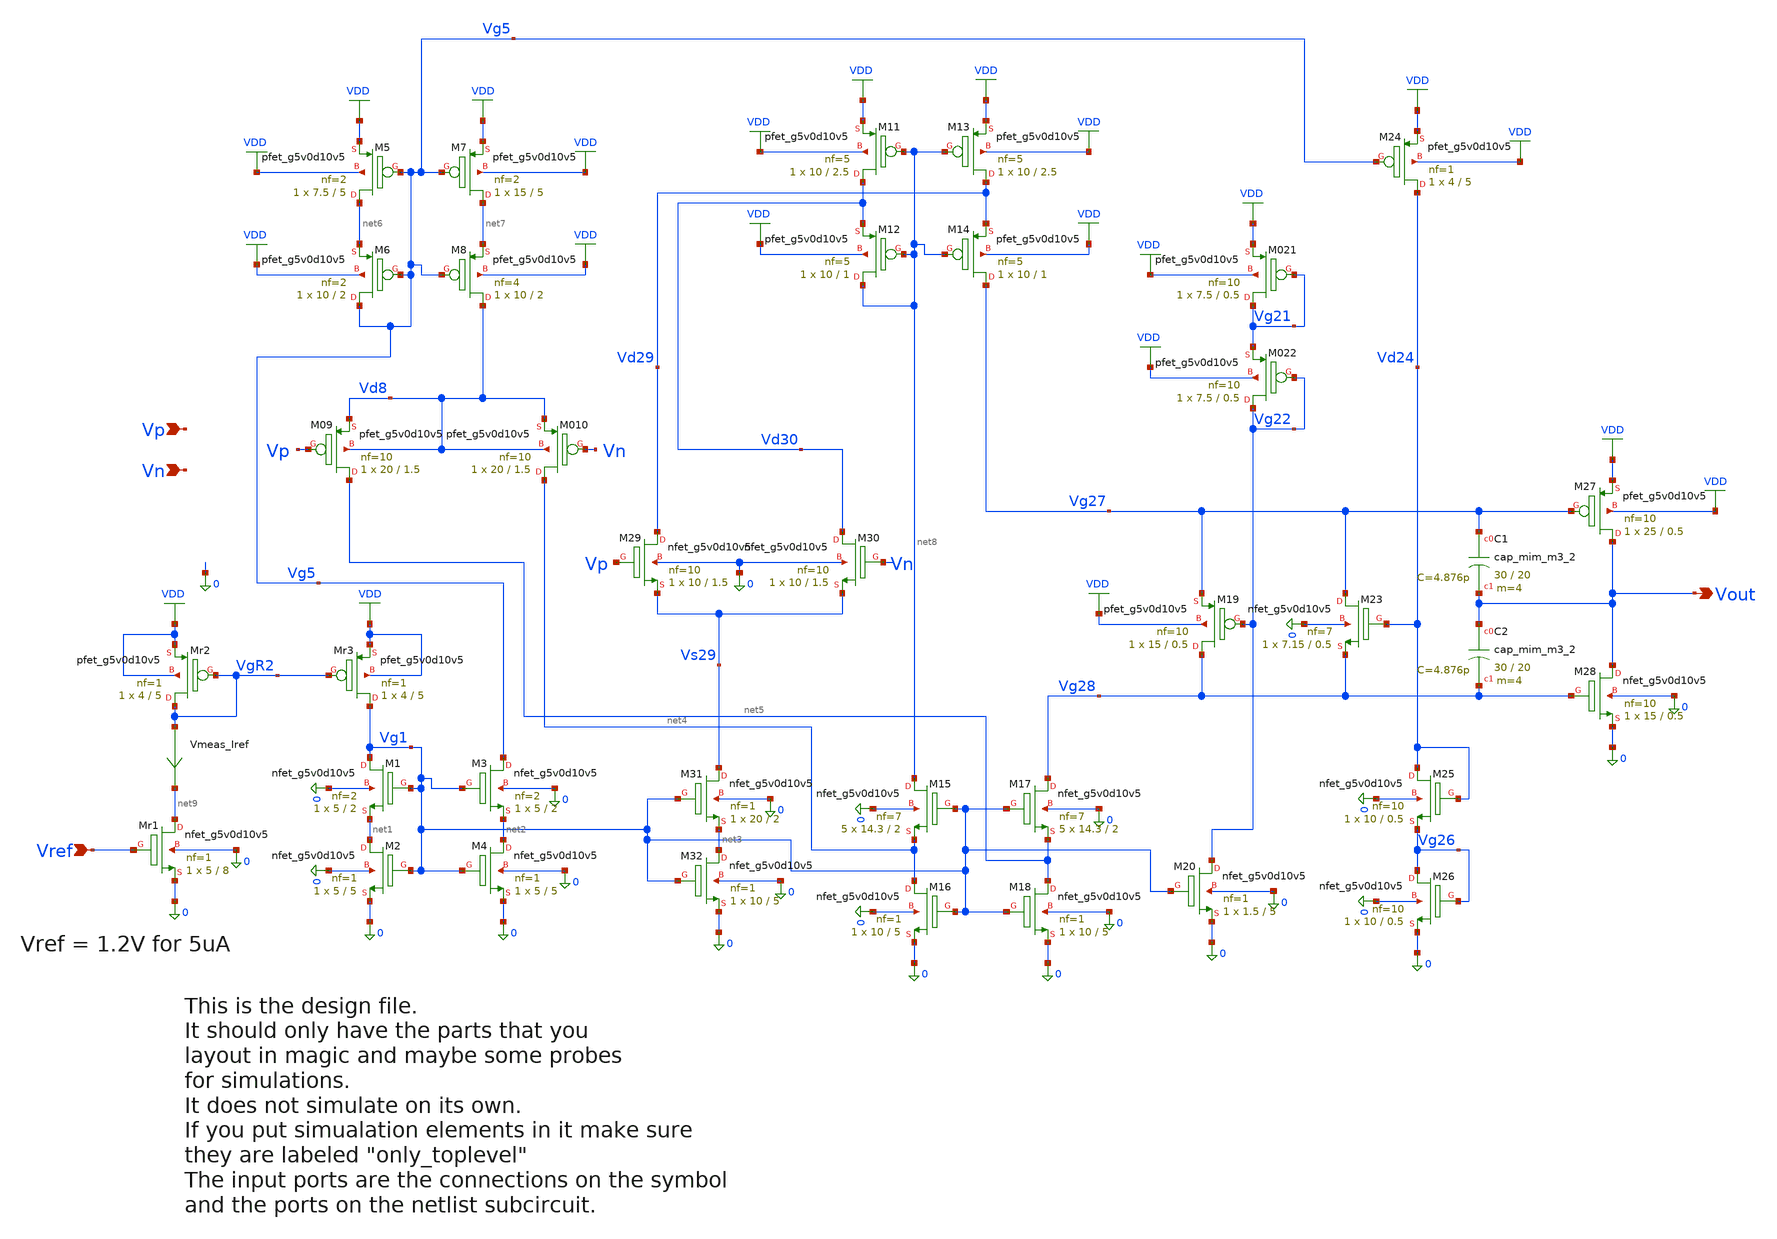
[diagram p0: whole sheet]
** sch_path: xschem/opamp_x_broken.sch
* Copyright 2021 Stefan Frederik Schippers
* Licensed under the Apache License, Version 2.0 (the "License");
* you may not use this file except in compliance with the License.
* You may obtain a copy of the License at
* https://www.apache.org/licenses/LICENSE-2.0
* Unless required by applicable law or agreed to in writing, software
* distributed under the License is distributed on an "AS IS" BASIS,
* WITHOUT WARRANTIES OR CONDITIONS OF ANY KIND, either express or implied.
* See the License for the specific language governing permissions and
* limitations under the License.
**.subckt opamp_x_broken Vout Vref Vp Vn
*.opin Vout
*.ipin Vref
*.ipin Vp
*.ipin Vn
XM1 Vg1 Vg1 net1 0 sky130_fd_pr__nfet_g5v0d10v5 L=2 W=5 nf=2 ad='int((2 + 1)/2) * 5 / 2 * 0.29' as='int((2 + 2)/2) * 5 / 2 * 0.29'
+ pd='2*int((2 + 1)/2) * (5 / 2 + 0.29)' ps='2*int((2 + 2)/2) * (5 / 2 + 0.29)' nrd='0.29 / 5 ' nrs='0.29 / 5 '
+ sa=0 sb=0 sd=0 mult=1 m=1
XM2 net1 Vg1 0 0 sky130_fd_pr__nfet_g5v0d10v5 L=5 W=5 nf=1 ad='int((1 + 1)/2) * 5 / 1 * 0.29' as='int((1 + 2)/2) * 5 / 1 * 0.29'
+ pd='2*int((1 + 1)/2) * (5 / 1 + 0.29)' ps='2*int((1 + 2)/2) * (5 / 1 + 0.29)' nrd='0.29 / 5 ' nrs='0.29 / 5 '
+ sa=0 sb=0 sd=0 mult=1 m=1
XM4 net2 Vg1 0 0 sky130_fd_pr__nfet_g5v0d10v5 L=5 W=5 nf=1 ad='int((1 + 1)/2) * 5 / 1 * 0.29' as='int((1 + 2)/2) * 5 / 1 * 0.29'
+ pd='2*int((1 + 1)/2) * (5 / 1 + 0.29)' ps='2*int((1 + 2)/2) * (5 / 1 + 0.29)' nrd='0.29 / 5 ' nrs='0.29 / 5 '
+ sa=0 sb=0 sd=0 mult=1 m=1
XM3 Vg5 Vg1 net2 0 sky130_fd_pr__nfet_g5v0d10v5 L=2 W=5 nf=2 ad='int((2 + 1)/2) * 5 / 2 * 0.29' as='int((2 + 2)/2) * 5 / 2 * 0.29'
+ pd='2*int((2 + 1)/2) * (5 / 2 + 0.29)' ps='2*int((2 + 2)/2) * (5 / 2 + 0.29)' nrd='0.29 / 5 ' nrs='0.29 / 5 '
+ sa=0 sb=0 sd=0 mult=1 m=1
XMr1 net9 Vref 0 0 sky130_fd_pr__nfet_g5v0d10v5 L=8 W=5 nf=1 ad='int((1 + 1)/2) * 5 / 1 * 0.29' as='int((1 + 2)/2) * 5 / 1 * 0.29'
+ pd='2*int((1 + 1)/2) * (5 / 1 + 0.29)' ps='2*int((1 + 2)/2) * (5 / 1 + 0.29)' nrd='0.29 / 5 ' nrs='0.29 / 5 '
+ sa=0 sb=0 sd=0 mult=1 m=1
XMr2 VgR2 VgR2 VDD VDD sky130_fd_pr__pfet_g5v0d10v5 L=5 W=4 nf=1 ad='int((1 + 1)/2) * 4 / 1 * 0.29' as='int((1 + 2)/2) * 4 / 1 * 0.29'
+ pd='2*int((1 + 1)/2) * (4 / 1 + 0.29)' ps='2*int((1 + 2)/2) * (4 / 1 + 0.29)' nrd='0.29 / 4 ' nrs='0.29 / 4 '
+ sa=0 sb=0 sd=0 mult=1 m=1
XMr3 Vg1 VgR2 VDD VDD sky130_fd_pr__pfet_g5v0d10v5 L=5 W=4 nf=1 ad='int((1 + 1)/2) * 4 / 1 * 0.29' as='int((1 + 2)/2) * 4 / 1 * 0.29'
+ pd='2*int((1 + 1)/2) * (4 / 1 + 0.29)' ps='2*int((1 + 2)/2) * (4 / 1 + 0.29)' nrd='0.29 / 4 ' nrs='0.29 / 4 '
+ sa=0 sb=0 sd=0 mult=1 m=1
XM32 net3 Vg1 0 0 sky130_fd_pr__nfet_g5v0d10v5 L=5 W=10 nf=1 ad='int((1 + 1)/2) * 10 / 1 * 0.29' as='int((1 + 2)/2) * 10 / 1 * 0.29'
+ pd='2*int((1 + 1)/2) * (10 / 1 + 0.29)' ps='2*int((1 + 2)/2) * (10 / 1 + 0.29)' nrd='0.29 / 10 ' nrs='0.29 / 10 '
+ sa=0 sb=0 sd=0 mult=1 m=1
XM31 Vs29 Vg1 net3 0 sky130_fd_pr__nfet_g5v0d10v5 L=2 W=20 nf=1 ad='int((1 + 1)/2) * 20 / 1 * 0.29' as='int((1 + 2)/2) * 20 / 1 * 0.29'
+ pd='2*int((1 + 1)/2) * (20 / 1 + 0.29)' ps='2*int((1 + 2)/2) * (20 / 1 + 0.29)' nrd='0.29 / 20 ' nrs='0.29 / 20 '
+ sa=0 sb=0 sd=0 mult=1 m=1
XM15 net8 Vg1 net4 0 sky130_fd_pr__nfet_g5v0d10v5 L=2 W=14.3 nf=7 ad='int((7 + 1)/2) * 14.3 / 7 * 0.29'
+ as='int((7 + 2)/2) * 14.3 / 7 * 0.29' pd='2*int((7 + 1)/2) * (14.3 / 7 + 0.29)' ps='2*int((7 + 2)/2) * (14.3 / 7 + 0.29)'
+ nrd='0.29 / 14.3 ' nrs='0.29 / 14.3 ' sa=0 sb=0 sd=0 mult=5 m=5
XM16 net4 Vg1 0 0 sky130_fd_pr__nfet_g5v0d10v5 L=5 W=10 nf=1 ad='int((1 + 1)/2) * 10 / 1 * 0.29' as='int((1 + 2)/2) * 10 / 1 * 0.29'
+ pd='2*int((1 + 1)/2) * (10 / 1 + 0.29)' ps='2*int((1 + 2)/2) * (10 / 1 + 0.29)' nrd='0.29 / 10 ' nrs='0.29 / 10 '
+ sa=0 sb=0 sd=0 mult=1 m=1
XM18 net5 Vg1 0 0 sky130_fd_pr__nfet_g5v0d10v5 L=5 W=10 nf=1 ad='int((1 + 1)/2) * 10 / 1 * 0.29' as='int((1 + 2)/2) * 10 / 1 * 0.29'
+ pd='2*int((1 + 1)/2) * (10 / 1 + 0.29)' ps='2*int((1 + 2)/2) * (10 / 1 + 0.29)' nrd='0.29 / 10 ' nrs='0.29 / 10 '
+ sa=0 sb=0 sd=0 mult=1 m=1
XM17 Vg28 Vg1 net5 0 sky130_fd_pr__nfet_g5v0d10v5 L=2 W=14.3 nf=7 ad='int((7 + 1)/2) * 14.3 / 7 * 0.29'
+ as='int((7 + 2)/2) * 14.3 / 7 * 0.29' pd='2*int((7 + 1)/2) * (14.3 / 7 + 0.29)' ps='2*int((7 + 2)/2) * (14.3 / 7 + 0.29)'
+ nrd='0.29 / 14.3 ' nrs='0.29 / 14.3 ' sa=0 sb=0 sd=0 mult=5 m=5
XM20 Vg22 Vg1 0 0 sky130_fd_pr__nfet_g5v0d10v5 L=5 W=1.5 nf=1 ad='int((1 + 1)/2) * 1.5 / 1 * 0.29' as='int((1 + 2)/2) * 1.5 / 1 * 0.29'
+ pd='2*int((1 + 1)/2) * (1.5 / 1 + 0.29)' ps='2*int((1 + 2)/2) * (1.5 / 1 + 0.29)' nrd='0.29 / 1.5 ' nrs='0.29 / 1.5 '
+ sa=0 sb=0 sd=0 mult=1 m=1
XM26 Vg26 Vg26 0 0 sky130_fd_pr__nfet_g5v0d10v5 L=0.5 W=10 nf=10 ad='int((10 + 1)/2) * 10 / 10 * 0.29'
+ as='int((10 + 2)/2) * 10 / 10 * 0.29' pd='2*int((10 + 1)/2) * (10 / 10 + 0.29)' ps='2*int((10 + 2)/2) * (10 / 10 + 0.29)'
+ nrd='0.29 / 10 ' nrs='0.29 / 10 ' sa=0 sb=0 sd=0 mult=1 m=1
XM25 Vd24 Vd24 Vg26 0 sky130_fd_pr__nfet_g5v0d10v5 L=0.5 W=10 nf=10 ad='int((10 + 1)/2) * 10 / 10 * 0.29'
+ as='int((10 + 2)/2) * 10 / 10 * 0.29' pd='2*int((10 + 1)/2) * (10 / 10 + 0.29)' ps='2*int((10 + 2)/2) * (10 / 10 + 0.29)'
+ nrd='0.29 / 10 ' nrs='0.29 / 10 ' sa=0 sb=0 sd=0 mult=1 m=1
XM23 Vg27 Vd24 Vg28 0 sky130_fd_pr__nfet_g5v0d10v5 L=0.5 W=7.15 nf=7 ad='int((7 + 1)/2) * 7.15 / 7 * 0.29'
+ as='int((7 + 2)/2) * 7.15 / 7 * 0.29' pd='2*int((7 + 1)/2) * (7.15 / 7 + 0.29)' ps='2*int((7 + 2)/2) * (7.15 / 7 + 0.29)'
+ nrd='0.29 / 7.15 ' nrs='0.29 / 7.15 ' sa=0 sb=0 sd=0 mult=1 m=1
XM28 Vout Vg28 0 0 sky130_fd_pr__nfet_g5v0d10v5 L=0.5 W=15 nf=10 ad='int((10 + 1)/2) * 15 / 10 * 0.29'
+ as='int((10 + 2)/2) * 15 / 10 * 0.29' pd='2*int((10 + 1)/2) * (15 / 10 + 0.29)' ps='2*int((10 + 2)/2) * (15 / 10 + 0.29)'
+ nrd='0.29 / 15 ' nrs='0.29 / 15 ' sa=0 sb=0 sd=0 mult=1 m=1
XM30 Vd30 Vn Vs29 0 sky130_fd_pr__nfet_g5v0d10v5 L=1.5 W=10 nf=10 ad='int((10 + 1)/2) * 10 / 10 * 0.29'
+ as='int((10 + 2)/2) * 10 / 10 * 0.29' pd='2*int((10 + 1)/2) * (10 / 10 + 0.29)' ps='2*int((10 + 2)/2) * (10 / 10 + 0.29)'
+ nrd='0.29 / 10 ' nrs='0.29 / 10 ' sa=0 sb=0 sd=0 mult=1 m=1
XM29 Vd29 Vp Vs29 0 sky130_fd_pr__nfet_g5v0d10v5 L=1.5 W=10 nf=10 ad='int((10 + 1)/2) * 10 / 10 * 0.29'
+ as='int((10 + 2)/2) * 10 / 10 * 0.29' pd='2*int((10 + 1)/2) * (10 / 10 + 0.29)' ps='2*int((10 + 2)/2) * (10 / 10 + 0.29)'
+ nrd='0.29 / 10 ' nrs='0.29 / 10 ' sa=0 sb=0 sd=0 mult=1 m=1
XM5 net6 Vg5 VDD VDD sky130_fd_pr__pfet_g5v0d10v5 L=5 W=7.5 nf=2 ad='int((2 + 1)/2) * 7.5 / 2 * 0.29'
+ as='int((2 + 2)/2) * 7.5 / 2 * 0.29' pd='2*int((2 + 1)/2) * (7.5 / 2 + 0.29)' ps='2*int((2 + 2)/2) * (7.5 / 2 + 0.29)'
+ nrd='0.29 / 7.5 ' nrs='0.29 / 7.5 ' sa=0 sb=0 sd=0 mult=1 m=1
XM6 Vg5 Vg5 net6 VDD sky130_fd_pr__pfet_g5v0d10v5 L=2 W=10 nf=2 ad='int((2 + 1)/2) * 10 / 2 * 0.29' as='int((2 + 2)/2) * 10 / 2 * 0.29'
+ pd='2*int((2 + 1)/2) * (10 / 2 + 0.29)' ps='2*int((2 + 2)/2) * (10 / 2 + 0.29)' nrd='0.29 / 10 ' nrs='0.29 / 10 '
+ sa=0 sb=0 sd=0 mult=1 m=1
XM7 net7 Vg5 VDD VDD sky130_fd_pr__pfet_g5v0d10v5 L=5 W=15 nf=2 ad='int((2 + 1)/2) * 15 / 2 * 0.29' as='int((2 + 2)/2) * 15 / 2 * 0.29'
+ pd='2*int((2 + 1)/2) * (15 / 2 + 0.29)' ps='2*int((2 + 2)/2) * (15 / 2 + 0.29)' nrd='0.29 / 15 ' nrs='0.29 / 15 '
+ sa=0 sb=0 sd=0 mult=1 m=1
XM8 Vd8 Vg5 net7 VDD sky130_fd_pr__pfet_g5v0d10v5 L=2 W=10 nf=4 ad='int((4 + 1)/2) * 10 / 4 * 0.29' as='int((4 + 2)/2) * 10 / 4 * 0.29'
+ pd='2*int((4 + 1)/2) * (10 / 4 + 0.29)' ps='2*int((4 + 2)/2) * (10 / 4 + 0.29)' nrd='0.29 / 10 ' nrs='0.29 / 10 '
+ sa=0 sb=0 sd=0 mult=1 m=1
XM09 net5 Vp Vd8 Vd8 sky130_fd_pr__pfet_g5v0d10v5 L=1.5 W=20 nf=10 ad='int((10 + 1)/2) * 20 / 10 * 0.29'
+ as='int((10 + 2)/2) * 20 / 10 * 0.29' pd='2*int((10 + 1)/2) * (20 / 10 + 0.29)' ps='2*int((10 + 2)/2) * (20 / 10 + 0.29)'
+ nrd='0.29 / 20 ' nrs='0.29 / 20 ' sa=0 sb=0 sd=0 mult=1 m=1
XM010 net4 Vn Vd8 Vd8 sky130_fd_pr__pfet_g5v0d10v5 L=1.5 W=20 nf=10 ad='int((10 + 1)/2) * 20 / 10 * 0.29'
+ as='int((10 + 2)/2) * 20 / 10 * 0.29' pd='2*int((10 + 1)/2) * (20 / 10 + 0.29)' ps='2*int((10 + 2)/2) * (20 / 10 + 0.29)'
+ nrd='0.29 / 20 ' nrs='0.29 / 20 ' sa=0 sb=0 sd=0 mult=1 m=1
XM13 Vd29 net8 VDD VDD sky130_fd_pr__pfet_g5v0d10v5 L=2.5 W=10 nf=5 ad='int((5 + 1)/2) * 10 / 5 * 0.29'
+ as='int((5 + 2)/2) * 10 / 5 * 0.29' pd='2*int((5 + 1)/2) * (10 / 5 + 0.29)' ps='2*int((5 + 2)/2) * (10 / 5 + 0.29)'
+ nrd='0.29 / 10 ' nrs='0.29 / 10 ' sa=0 sb=0 sd=0 mult=1 m=1
XM14 Vg27 net8 Vd29 VDD sky130_fd_pr__pfet_g5v0d10v5 L=1 W=10 nf=5 ad='int((5 + 1)/2) * 10 / 5 * 0.29'
+ as='int((5 + 2)/2) * 10 / 5 * 0.29' pd='2*int((5 + 1)/2) * (10 / 5 + 0.29)' ps='2*int((5 + 2)/2) * (10 / 5 + 0.29)'
+ nrd='0.29 / 10 ' nrs='0.29 / 10 ' sa=0 sb=0 sd=0 mult=1 m=1
XM11 Vd30 net8 VDD VDD sky130_fd_pr__pfet_g5v0d10v5 L=2.5 W=10 nf=5 ad='int((5 + 1)/2) * 10 / 5 * 0.29'
+ as='int((5 + 2)/2) * 10 / 5 * 0.29' pd='2*int((5 + 1)/2) * (10 / 5 + 0.29)' ps='2*int((5 + 2)/2) * (10 / 5 + 0.29)'
+ nrd='0.29 / 10 ' nrs='0.29 / 10 ' sa=0 sb=0 sd=0 mult=1 m=1
XM12 net8 net8 Vd30 VDD sky130_fd_pr__pfet_g5v0d10v5 L=1 W=10 nf=5 ad='int((5 + 1)/2) * 10 / 5 * 0.29'
+ as='int((5 + 2)/2) * 10 / 5 * 0.29' pd='2*int((5 + 1)/2) * (10 / 5 + 0.29)' ps='2*int((5 + 2)/2) * (10 / 5 + 0.29)'
+ nrd='0.29 / 10 ' nrs='0.29 / 10 ' sa=0 sb=0 sd=0 mult=1 m=1
XM021 Vg21 Vg21 VDD VDD sky130_fd_pr__pfet_g5v0d10v5 L=0.5 W=7.5 nf=10 ad='int((10 + 1)/2) * 7.5 / 10 * 0.29'
+ as='int((10 + 2)/2) * 7.5 / 10 * 0.29' pd='2*int((10 + 1)/2) * (7.5 / 10 + 0.29)' ps='2*int((10 + 2)/2) * (7.5 / 10 + 0.29)'
+ nrd='0.29 / 7.5 ' nrs='0.29 / 7.5 ' sa=0 sb=0 sd=0 mult=1 m=1
XM022 Vg22 Vg22 Vg21 VDD sky130_fd_pr__pfet_g5v0d10v5 L=0.5 W=7.5 nf=10 ad='int((10 + 1)/2) * 7.5 / 10 * 0.29'
+ as='int((10 + 2)/2) * 7.5 / 10 * 0.29' pd='2*int((10 + 1)/2) * (7.5 / 10 + 0.29)' ps='2*int((10 + 2)/2) * (7.5 / 10 + 0.29)'
+ nrd='0.29 / 7.5 ' nrs='0.29 / 7.5 ' sa=0 sb=0 sd=0 mult=1 m=1
XM24 Vd24 Vg5 VDD VDD sky130_fd_pr__pfet_g5v0d10v5 L=5 W=4 nf=1 ad='int((1 + 1)/2) * 4 / 1 * 0.29' as='int((1 + 2)/2) * 4 / 1 * 0.29'
+ pd='2*int((1 + 1)/2) * (4 / 1 + 0.29)' ps='2*int((1 + 2)/2) * (4 / 1 + 0.29)' nrd='0.29 / 4 ' nrs='0.29 / 4 '
+ sa=0 sb=0 sd=0 mult=1 m=1
XM27 Vout Vg27 VDD VDD sky130_fd_pr__pfet_g5v0d10v5 L=0.5 W=25 nf=10 ad='int((10 + 1)/2) * 25 / 10 * 0.29'
+ as='int((10 + 2)/2) * 25 / 10 * 0.29' pd='2*int((10 + 1)/2) * (25 / 10 + 0.29)' ps='2*int((10 + 2)/2) * (25 / 10 + 0.29)'
+ nrd='0.29 / 25 ' nrs='0.29 / 25 ' sa=0 sb=0 sd=0 mult=1 m=1
XC1 Vg27 Vout sky130_fd_pr__cap_mim_m3_2 W=30 L=20 MF=4 m=4
XC2 Vout Vg28 sky130_fd_pr__cap_mim_m3_2 W=30 L=20 MF=4 m=4
XM19 Vg28 Vg22 Vg27 VDD sky130_fd_pr__pfet_g5v0d10v5 L=0.5 W=15 nf=10 ad='int((10 + 1)/2) * 15 / 10 * 0.29'
+ as='int((10 + 2)/2) * 15 / 10 * 0.29' pd='2*int((10 + 1)/2) * (15 / 10 + 0.29)' ps='2*int((10 + 2)/2) * (15 / 10 + 0.29)'
+ nrd='0.29 / 15 ' nrs='0.29 / 15 ' sa=0 sb=0 sd=0 mult=1 m=1
Vmeas_Iref VgR2 net9 0
.save i(vmeas_iref)
**.ends
.GLOBAL VDD
.end
